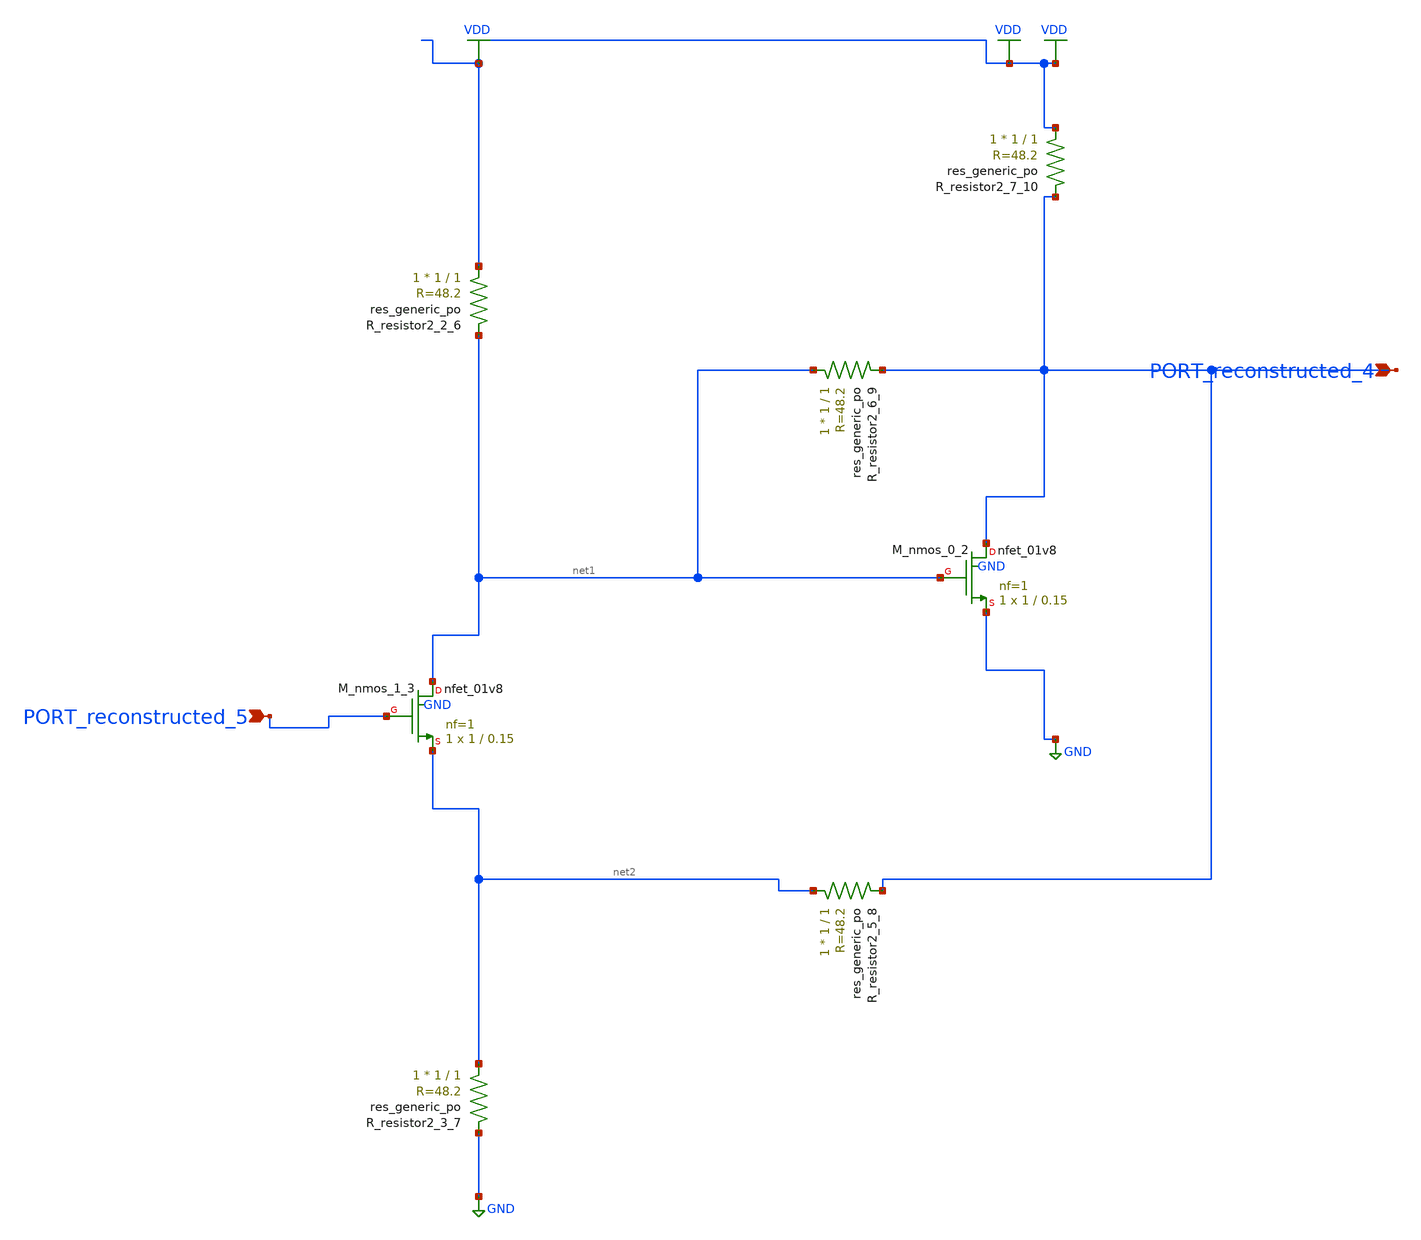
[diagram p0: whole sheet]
** sch_path: schematics/AMSNet/618.sch
**.subckt 618 PORT_reconstructed_4 PORT_reconstructed_5
*.ipin PORT_reconstructed_4
*.ipin PORT_reconstructed_5
XM_nmos_0_2 PORT_reconstructed_4 net1 GND GND sky130_fd_pr__nfet_01v8 L=0.15 W=1 nf=1 ad='int((1 + 1)/2) * 1 / 1 * 0.29'
+ as='int((1 + 2)/2) * 1 / 1 * 0.29' pd='2*int((1 + 1)/2) * (1 / 1 + 0.29)' ps='2*int((1 + 2)/2) * (1 / 1 + 0.29)'
+ nrd='0.29 / 1 ' nrs='0.29 / 1 ' sa=0 sb=0 sd=0 mult=1 m=1
XM_nmos_1_3 net1 PORT_reconstructed_5 net2 GND sky130_fd_pr__nfet_01v8 L=0.15 W=1 nf=1 ad='int((1 + 1)/2) * 1 / 1 * 0.29'
+ as='int((1 + 2)/2) * 1 / 1 * 0.29' pd='2*int((1 + 1)/2) * (1 / 1 + 0.29)' ps='2*int((1 + 2)/2) * (1 / 1 + 0.29)'
+ nrd='0.29 / 1 ' nrs='0.29 / 1 ' sa=0 sb=0 sd=0 mult=1 m=1
XR_resistor2_2_6 VDD net1 sky130_fd_pr__res_generic_po W=1 L=1 m=1
XR_resistor2_3_7 net2 GND sky130_fd_pr__res_generic_po W=1 L=1 m=1
XR_resistor2_5_8 net2 PORT_reconstructed_4 sky130_fd_pr__res_generic_po W=1 L=1 m=1
XR_resistor2_6_9 net1 PORT_reconstructed_4 sky130_fd_pr__res_generic_po W=1 L=1 m=1
XR_resistor2_7_10 VDD PORT_reconstructed_4 sky130_fd_pr__res_generic_po W=1 L=1 m=1
**.ends
.GLOBAL GND
.GLOBAL VDD
.end
